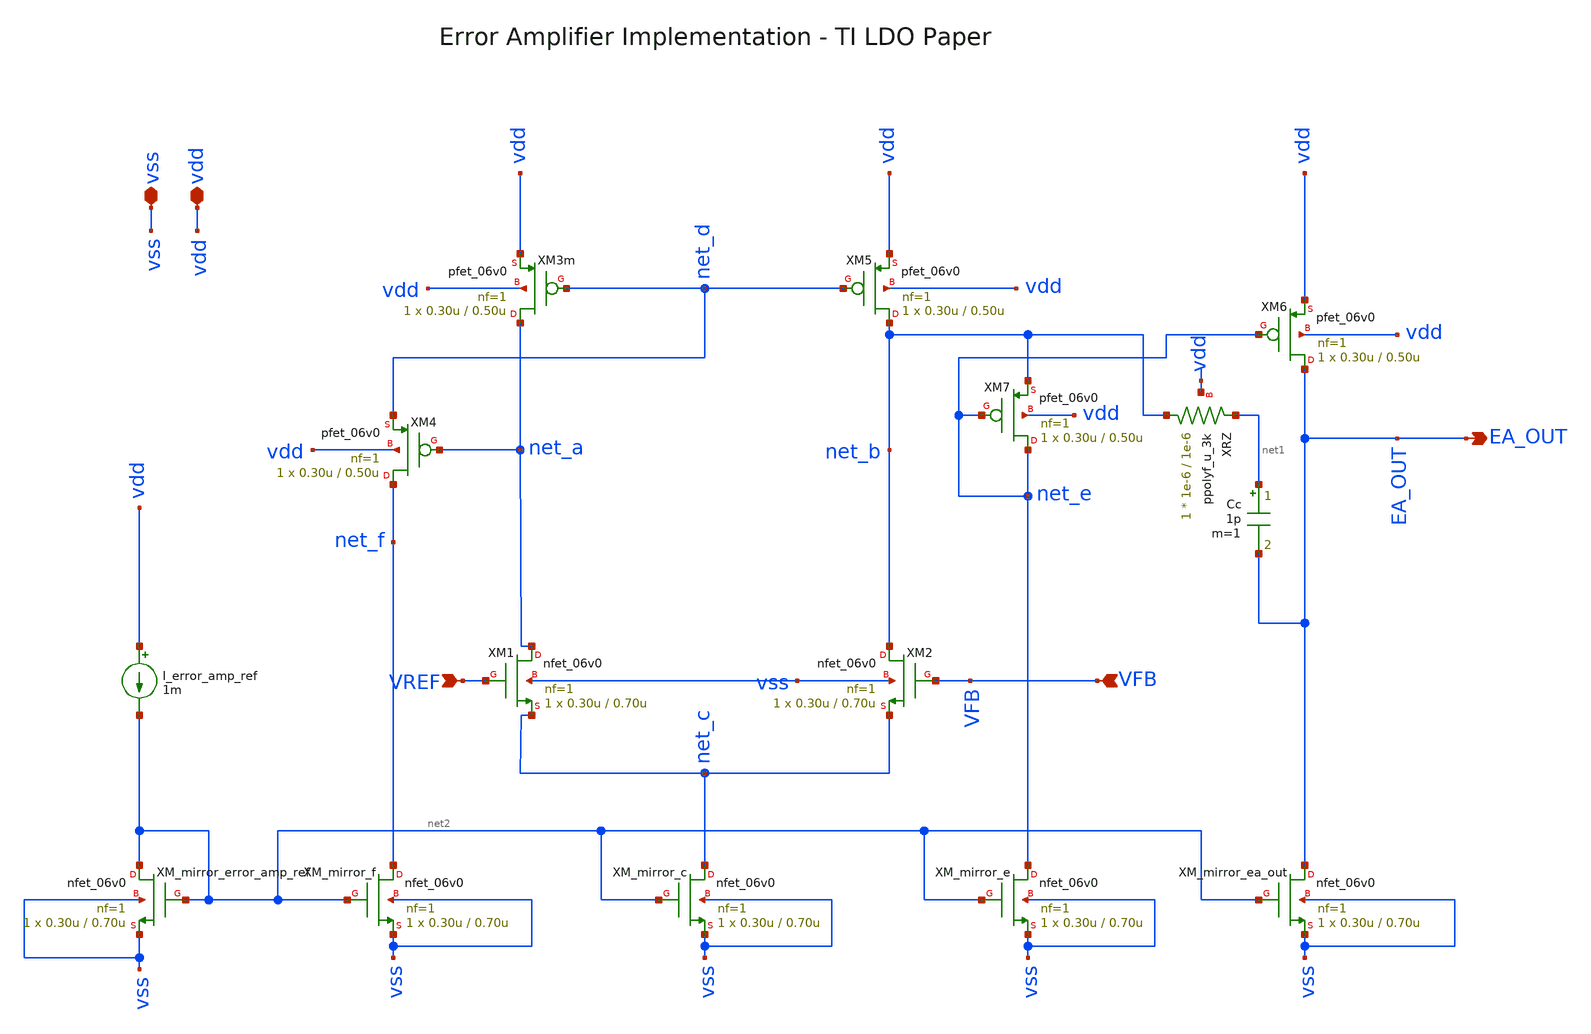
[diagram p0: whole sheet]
** sch_path: analog-db/circuits/ldo_005_buffered_ref/reference/ti-ldo/error_amp/error_amp.sch
**.subckt error_amp vdd vss VFB EA_OUT VREF
*.iopin vdd
*.iopin vss
*.ipin VFB
*.opin EA_OUT
*.ipin VREF
XM2 net_b VFB net_c vss nfet_06v0 L=0.70u W=0.30u nf=1 ad='int((nf+1)/2) * W/nf * 0.18u' as='int((nf+2)/2) * W/nf * 0.18u'
+ pd='2*int((nf+1)/2) * (W/nf + 0.18u)' ps='2*int((nf+2)/2) * (W/nf + 0.18u)' nrd='0.18u / W' nrs='0.18u / W'
+ sa=0 sb=0 sd=0 m=1
I_error_amp_ref vdd net2 1m
XM3m net_a net_d vdd vdd pfet_06v0 L=0.50u W=0.30u nf=1 ad='int((nf+1)/2) * W/nf * 0.18u' as='int((nf+2)/2) * W/nf * 0.18u'
+ pd='2*int((nf+1)/2) * (W/nf + 0.18u)' ps='2*int((nf+2)/2) * (W/nf + 0.18u)' nrd='0.18u / W' nrs='0.18u / W'
+ sa=0 sb=0 sd=0 m=1
XM4 net_f net_a net_d vdd pfet_06v0 L=0.50u W=0.30u nf=1 ad='int((nf+1)/2) * W/nf * 0.18u' as='int((nf+2)/2) * W/nf * 0.18u'
+ pd='2*int((nf+1)/2) * (W/nf + 0.18u)' ps='2*int((nf+2)/2) * (W/nf + 0.18u)' nrd='0.18u / W' nrs='0.18u / W'
+ sa=0 sb=0 sd=0 m=1
XM5 net_b net_d vdd vdd pfet_06v0 L=0.50u W=0.30u nf=1 ad='int((nf+1)/2) * W/nf * 0.18u' as='int((nf+2)/2) * W/nf * 0.18u'
+ pd='2*int((nf+1)/2) * (W/nf + 0.18u)' ps='2*int((nf+2)/2) * (W/nf + 0.18u)' nrd='0.18u / W' nrs='0.18u / W'
+ sa=0 sb=0 sd=0 m=1
XM6 EA_OUT net_e vdd vdd pfet_06v0 L=0.50u W=0.30u nf=1 ad='int((nf+1)/2) * W/nf * 0.18u' as='int((nf+2)/2) * W/nf * 0.18u'
+ pd='2*int((nf+1)/2) * (W/nf + 0.18u)' ps='2*int((nf+2)/2) * (W/nf + 0.18u)' nrd='0.18u / W' nrs='0.18u / W'
+ sa=0 sb=0 sd=0 m=1
XM7 net_e net_e net_b vdd pfet_06v0 L=0.50u W=0.30u nf=1 ad='int((nf+1)/2) * W/nf * 0.18u' as='int((nf+2)/2) * W/nf * 0.18u'
+ pd='2*int((nf+1)/2) * (W/nf + 0.18u)' ps='2*int((nf+2)/2) * (W/nf + 0.18u)' nrd='0.18u / W' nrs='0.18u / W'
+ sa=0 sb=0 sd=0 m=1
Cc net1 EA_OUT 1p m=1
XRZ net_b net1 vdd ppolyf_u_3k r_width=1e-6 r_length=1e-6 m=1
XM1 net_a VREF net_c vss nfet_06v0 L=0.70u W=0.30u nf=1 ad='int((nf+1)/2) * W/nf * 0.18u' as='int((nf+2)/2) * W/nf * 0.18u'
+ pd='2*int((nf+1)/2) * (W/nf + 0.18u)' ps='2*int((nf+2)/2) * (W/nf + 0.18u)' nrd='0.18u / W' nrs='0.18u / W'
+ sa=0 sb=0 sd=0 m=1
XM_mirror_error_amp_ref net2 net2 vss vss nfet_06v0 L=0.70u W=0.30u nf=1 ad='int((nf+1)/2) * W/nf * 0.18u'
+ as='int((nf+2)/2) * W/nf * 0.18u' pd='2*int((nf+1)/2) * (W/nf + 0.18u)' ps='2*int((nf+2)/2) * (W/nf + 0.18u)'
+ nrd='0.18u / W' nrs='0.18u / W' sa=0 sb=0 sd=0 m=1
XM_mirror_f net_f net2 vss vss nfet_06v0 L=0.70u W=0.30u nf=1 ad='int((nf+1)/2) * W/nf * 0.18u' as='int((nf+2)/2) * W/nf * 0.18u'
+ pd='2*int((nf+1)/2) * (W/nf + 0.18u)' ps='2*int((nf+2)/2) * (W/nf + 0.18u)' nrd='0.18u / W' nrs='0.18u / W'
+ sa=0 sb=0 sd=0 m=1
XM_mirror_c net_c net2 vss vss nfet_06v0 L=0.70u W=0.30u nf=1 ad='int((nf+1)/2) * W/nf * 0.18u' as='int((nf+2)/2) * W/nf * 0.18u'
+ pd='2*int((nf+1)/2) * (W/nf + 0.18u)' ps='2*int((nf+2)/2) * (W/nf + 0.18u)' nrd='0.18u / W' nrs='0.18u / W'
+ sa=0 sb=0 sd=0 m=1
XM_mirror_e net_e net2 vss vss nfet_06v0 L=0.70u W=0.30u nf=1 ad='int((nf+1)/2) * W/nf * 0.18u' as='int((nf+2)/2) * W/nf * 0.18u'
+ pd='2*int((nf+1)/2) * (W/nf + 0.18u)' ps='2*int((nf+2)/2) * (W/nf + 0.18u)' nrd='0.18u / W' nrs='0.18u / W'
+ sa=0 sb=0 sd=0 m=1
XM_mirror_ea_out EA_OUT net2 vss vss nfet_06v0 L=0.70u W=0.30u nf=1 ad='int((nf+1)/2) * W/nf * 0.18u'
+ as='int((nf+2)/2) * W/nf * 0.18u' pd='2*int((nf+1)/2) * (W/nf + 0.18u)' ps='2*int((nf+2)/2) * (W/nf + 0.18u)'
+ nrd='0.18u / W' nrs='0.18u / W' sa=0 sb=0 sd=0 m=1
**** begin user architecture code

** Error Amp Parameters **

.param I_error_amp_ref = 1m


** Passive Devices
.param C_error_amp_cc 	= 100p

.param R_error_amp_rz_w	= 1e-6
.param R_error_amp_rz_l	= 1e-6

** NMOS
** error_amp.M1 Transistor
.param M1_error_amp_nfet_w  = 0.50u
.param M1_error_amp_nfet_l  = 0.30u
.param M1_error_amp_nfet_nf = 1
.param M1_error_amp_nfet_m  = 1

** error_amp.M2 Transistor
.param M2_error_amp_nfet_w  = 0.50u
.param M2_error_amp_nfet_l  = 0.30u
.param M2_error_amp_nfet_nf = 1
.param M2_error_amp_nfet_m  = 1

** error_amp.M_mirror_ea_out Transistor
.param M_mirror_ea_out_error_amp_nfet_w  = 0.50u
.param M_mirror_ea_out_error_amp_nfet_l  = 0.30u
.param M_mirror_ea_out_error_amp_nfet_nf = 1
.param M_mirror_ea_out_error_amp_nfet_m  = 1

** error_amp.M_mirror_e Transistor
.param M_mirror_e_error_amp_nfet_w  = 0.50u
.param M_mirror_e_error_amp_nfet_l  = 0.30u
.param M_mirror_e_error_amp_nfet_nf = 1
.param M_mirror_e_error_amp_nfet_m  = 1

** error_amp.M_mirror_c Transistor
.param M_mirror_c_error_amp_nfet_w  = 0.50u
.param M_mirror_c_error_amp_nfet_l  = 0.30u
.param M_mirror_c_error_amp_nfet_nf = 1
.param M_mirror_c_error_amp_nfet_m  = 1

** error_amp.M_mirror_f Transistor
.param M_mirror_f_error_amp_nfet_w  = 0.50u
.param M_mirror_f_error_amp_nfet_l  = 0.30u
.param M_mirror_f_error_amp_nfet_nf = 1
.param M_mirror_f_error_amp_nfet_m  = 1

** error_amp.M_mirror_error_amp_ref Transistor
.param M_mirror_error_amp_ref_error_amp_nfet_w  = 0.50u
.param M_mirror_error_amp_ref_error_amp_nfet_l  = 0.30u
.param M_mirror_error_amp_ref_error_amp_nfet_nf = 1
.param M_mirror_error_amp_ref_error_amp_nfet_m  = 1

** PMOS
** error_amp.M3 Transistor
.param M3_error_amp_pfet_w  = 0.50u
.param M3_error_amp_pfet_l  = 0.30u
.param M3_error_amp_pfet_nf = 1
.param M3_error_amp_pfet_m  = 1

** error_amp.M4 Transistor
.param M4_error_amp_pfet_w  = 0.50u
.param M4_error_amp_pfet_l  = 0.30u
.param M4_error_amp_pfet_nf = 1
.param M4_error_amp_pfet_m  = 1

** error_amp.M5 Transistor
.param M5_error_amp_pfet_w  = 0.50u
.param M5_error_amp_pfet_l  = 0.30u
.param M5_error_amp_pfet_nf = 1
.param M5_error_amp_pfet_m  = 1

** error_amp.M6 Transistor
.param M6_error_amp_pfet_w  = 0.50u
.param M6_error_amp_pfet_l  = 0.30u
.param M6_error_amp_pfet_nf = 1
.param M6_error_amp_pfet_m  = 1

** error_amp.M7 Transistor
.param M7_error_amp_pfet_w  = 0.50u
.param M7_error_amp_pfet_l  = 0.30u
.param M7_error_amp_pfet_nf = 1
.param M7_error_amp_pfet_m  = 1


**** end user architecture code
**.ends
.end
